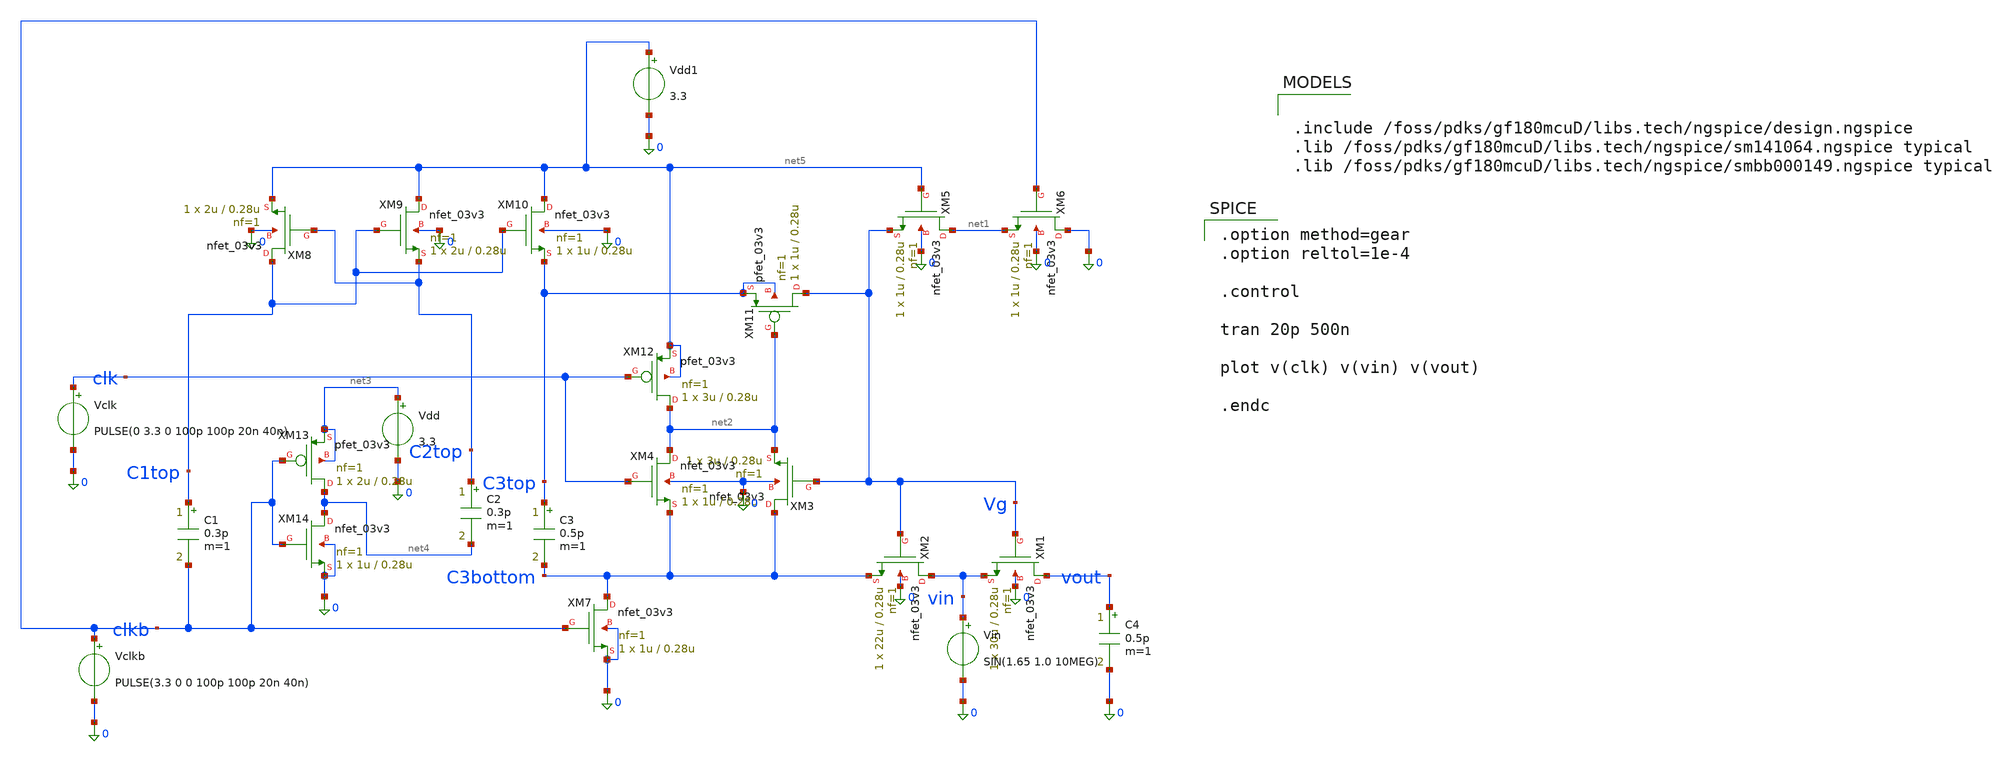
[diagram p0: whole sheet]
** sch_path: analog/blocks/Bootstrapped_Switch/bootstrapped_switch.sch
**.subckt bootstrapped_switch
XM1 vout Vg vin 0 nfet_03v3 L=0.28u W=30u nf=1 ad='int((nf+1)/2) * W/nf * 0.18u' as='int((nf+2)/2) * W/nf * 0.18u'
+ pd='2*int((nf+1)/2) * (W/nf + 0.18u)' ps='2*int((nf+2)/2) * (W/nf + 0.18u)' nrd='0.18u / W' nrs='0.18u / W'
+ sa=0 sb=0 sd=0 m=1
XM2 vin Vg C3bottom 0 nfet_03v3 L=0.28u W=22u nf=1 ad='int((nf+1)/2) * W/nf * 0.18u' as='int((nf+2)/2) * W/nf * 0.18u'
+ pd='2*int((nf+1)/2) * (W/nf + 0.18u)' ps='2*int((nf+2)/2) * (W/nf + 0.18u)' nrd='0.18u / W' nrs='0.18u / W'
+ sa=0 sb=0 sd=0 m=1
XM3 C3bottom Vg net2 0 nfet_03v3 L=0.28u W=3u nf=1 ad='int((nf+1)/2) * W/nf * 0.18u' as='int((nf+2)/2) * W/nf * 0.18u'
+ pd='2*int((nf+1)/2) * (W/nf + 0.18u)' ps='2*int((nf+2)/2) * (W/nf + 0.18u)' nrd='0.18u / W' nrs='0.18u / W'
+ sa=0 sb=0 sd=0 m=1
XM4 net2 clk C3bottom 0 nfet_03v3 L=0.28u W=1u nf=1 ad='int((nf+1)/2) * W/nf * 0.18u' as='int((nf+2)/2) * W/nf * 0.18u'
+ pd='2*int((nf+1)/2) * (W/nf + 0.18u)' ps='2*int((nf+2)/2) * (W/nf + 0.18u)' nrd='0.18u / W' nrs='0.18u / W'
+ sa=0 sb=0 sd=0 m=1
XM5 net1 net5 Vg 0 nfet_03v3 L=0.28u W=1u nf=1 ad='int((nf+1)/2) * W/nf * 0.18u' as='int((nf+2)/2) * W/nf * 0.18u'
+ pd='2*int((nf+1)/2) * (W/nf + 0.18u)' ps='2*int((nf+2)/2) * (W/nf + 0.18u)' nrd='0.18u / W' nrs='0.18u / W'
+ sa=0 sb=0 sd=0 m=1
XM6 0 clkb net1 0 nfet_03v3 L=0.28u W=1u nf=1 ad='int((nf+1)/2) * W/nf * 0.18u' as='int((nf+2)/2) * W/nf * 0.18u'
+ pd='2*int((nf+1)/2) * (W/nf + 0.18u)' ps='2*int((nf+2)/2) * (W/nf + 0.18u)' nrd='0.18u / W' nrs='0.18u / W'
+ sa=0 sb=0 sd=0 m=1
XM7 C3bottom clkb 0 0 nfet_03v3 L=0.28u W=1u nf=1 ad='int((nf+1)/2) * W/nf * 0.18u' as='int((nf+2)/2) * W/nf * 0.18u'
+ pd='2*int((nf+1)/2) * (W/nf + 0.18u)' ps='2*int((nf+2)/2) * (W/nf + 0.18u)' nrd='0.18u / W' nrs='0.18u / W'
+ sa=0 sb=0 sd=0 m=1
XM8 C1top C2top net5 0 nfet_03v3 L=0.28u W=2u nf=1 ad='int((nf+1)/2) * W/nf * 0.18u' as='int((nf+2)/2) * W/nf * 0.18u'
+ pd='2*int((nf+1)/2) * (W/nf + 0.18u)' ps='2*int((nf+2)/2) * (W/nf + 0.18u)' nrd='0.18u / W' nrs='0.18u / W'
+ sa=0 sb=0 sd=0 m=1
XM9 net5 C1top C2top 0 nfet_03v3 L=0.28u W=2u nf=1 ad='int((nf+1)/2) * W/nf * 0.18u' as='int((nf+2)/2) * W/nf * 0.18u'
+ pd='2*int((nf+1)/2) * (W/nf + 0.18u)' ps='2*int((nf+2)/2) * (W/nf + 0.18u)' nrd='0.18u / W' nrs='0.18u / W'
+ sa=0 sb=0 sd=0 m=1
XM10 net5 C1top C3top 0 nfet_03v3 L=0.28u W=1u nf=1 ad='int((nf+1)/2) * W/nf * 0.18u' as='int((nf+2)/2) * W/nf * 0.18u'
+ pd='2*int((nf+1)/2) * (W/nf + 0.18u)' ps='2*int((nf+2)/2) * (W/nf + 0.18u)' nrd='0.18u / W' nrs='0.18u / W'
+ sa=0 sb=0 sd=0 m=1
XM11 Vg net2 C3top C3top pfet_03v3 L=0.28u W=1u nf=1 ad='int((nf+1)/2) * W/nf * 0.18u' as='int((nf+2)/2) * W/nf * 0.18u'
+ pd='2*int((nf+1)/2) * (W/nf + 0.18u)' ps='2*int((nf+2)/2) * (W/nf + 0.18u)' nrd='0.18u / W' nrs='0.18u / W'
+ sa=0 sb=0 sd=0 m=1
XM12 net2 clk net5 net5 pfet_03v3 L=0.28u W=3u nf=1 ad='int((nf+1)/2) * W/nf * 0.18u' as='int((nf+2)/2) * W/nf * 0.18u'
+ pd='2*int((nf+1)/2) * (W/nf + 0.18u)' ps='2*int((nf+2)/2) * (W/nf + 0.18u)' nrd='0.18u / W' nrs='0.18u / W'
+ sa=0 sb=0 sd=0 m=1
C1 C1top clkb 0.3p m=1
C2 C2top net4 0.3p m=1
C3 C3top C3bottom 0.5p m=1
XM13 net4 clkb net3 net3 pfet_03v3 L=0.28u W=2u nf=1 ad='int((nf+1)/2) * W/nf * 0.18u' as='int((nf+2)/2) * W/nf * 0.18u'
+ pd='2*int((nf+1)/2) * (W/nf + 0.18u)' ps='2*int((nf+2)/2) * (W/nf + 0.18u)' nrd='0.18u / W' nrs='0.18u / W'
+ sa=0 sb=0 sd=0 m=1
XM14 net4 clkb 0 0 nfet_03v3 L=0.28u W=1u nf=1 ad='int((nf+1)/2) * W/nf * 0.18u' as='int((nf+2)/2) * W/nf * 0.18u'
+ pd='2*int((nf+1)/2) * (W/nf + 0.18u)' ps='2*int((nf+2)/2) * (W/nf + 0.18u)' nrd='0.18u / W' nrs='0.18u / W'
+ sa=0 sb=0 sd=0 m=1
Vdd net3 0 3.3
Vdd1 net5 0 3.3
Vclk clk 0 PULSE(0 3.3 0 100p 100p 20n 40n)
Vclkb clkb 0 PULSE(3.3 0 0 100p 100p 20n 40n)
Vin vin 0 SIN(1.65 1.0 10MEG)
C4 vout 0 0.5p m=1
**** begin user architecture code


.include /foss/pdks/gf180mcuD/libs.tech/ngspice/design.ngspice
.lib /foss/pdks/gf180mcuD/libs.tech/ngspice/sm141064.ngspice typical
.lib /foss/pdks/gf180mcuD/libs.tech/ngspice/smbb000149.ngspice typical


.option method=gear
.option reltol=1e-4

.control

tran 20p 500n

plot v(clk) v(vin) v(vout)

.endc

**** end user architecture code
**.ends
.end
